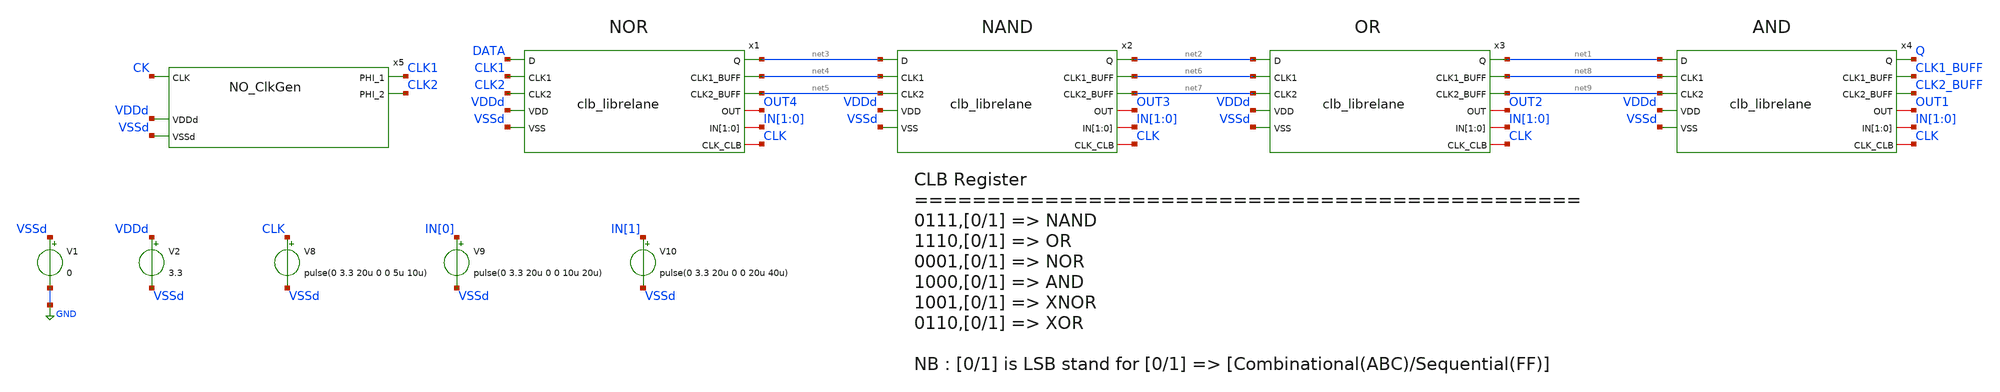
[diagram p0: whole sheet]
** sch_path: designs/libs/tb_fpga/tb_clb/tb_clb.sch
**.subckt tb_clb
V1 VSSd GND 0
V2 VDDd VSSd 3.3
V8 CLK VSSd pulse(0 3.3 20u 0 0 5u 10u)
V9 IN[0] VSSd pulse(0 3.3 20u 0 0 10u 20u)
V10 IN[1] VSSd pulse(0 3.3 20u 0 0 20u 40u)
x5 CLK2 CK CLK1 VDDd VSSd NO_ClkGen
x1 DATA CLK1 CLK2 VDDd VSSd net3 net4 net5 OUT4 IN[1] IN[0] CLK clb_librelane
x2 net3 net4 net5 VDDd VSSd net2 net6 net7 OUT3 IN[1] IN[0] CLK clb_librelane
x3 net2 net6 net7 VDDd VSSd net1 net8 net9 OUT2 IN[1] IN[0] CLK clb_librelane
x4 net1 net8 net9 VDDd VSSd Q CLK1_BUFF CLK2_BUFF OUT1 IN[1] IN[0] CLK clb_librelane
**** begin user architecture code


* clock
abit [ bit_node ]  input_vector
.model input_vector
+ d_source(input_file="/foss/designs/sscs-chipathon2025-LNA/designs/libs/tb_fpga/tb_clb/data.txt")
* data
aclock [ clock_node ] clock_vector
.model clock_vector
+ d_source(input_file="/foss/designs/sscs-chipathon2025-LNA/designs/libs/tb_fpga/tb_clb/data_clk.txt")
* convert digital signals to analog
aconvert [ bit_node clock_node ] [ data ck ] dac_in
.model dac_in dac_bridge (out_low=0V out_high=3.3V t_rise=0.2ns t_fall=0.2ns)

.control
    save all
    TRAN 0.1u 100u
    write tb_clb.raw
.endc



.include /foss/pdks/gf180mcuD/libs.ref/gf180mcu_fd_sc_mcu7t5v0/spice/gf180mcu_fd_sc_mcu7t5v0.spice
.include /foss/pdks/gf180mcuD/libs.ref/gf180mcu_fd_sc_mcu9t5v0/spice/gf180mcu_fd_sc_mcu9t5v0.spice
.include $::180MCU_MODELS/design.ngspice
.lib $::180MCU_MODELS/sm141064.ngspice typical

**** end user architecture code
**.ends

* expanding   symbol:  switch_matrix_gf180mcu_9t5v0/NO_ClkGen/NO_ClkGen.sym # of pins=5
** sym_path: switch_matrix_gf180mcu_9t5v0/NO_ClkGen/NO_ClkGen.sym
** sch_path: switch_matrix_gf180mcu_9t5v0/NO_ClkGen/NO_ClkGen.sch
.subckt NO_ClkGen PHI_2 CLK PHI_1 VDDd VSSd
*.ipin CLK
*.opin PHI_2
*.opin PHI_1
*.iopin VDDd
*.iopin VSSd
x1 OUT_bot_d CLKB VSSd VDDd VSSd VDDd OUT_top gf180mcu_fd_sc_mcu9t5v0__nand2_1
x2 OUT_top_d CLKbuf VSSd VDDd VSSd VDDd OUT_bot gf180mcu_fd_sc_mcu9t5v0__nand2_1
x3 OUT_top VSSd VDDd VSSd VDDd PHI_2 gf180mcu_fd_sc_mcu9t5v0__inv_1
x4 PHI_2 VSSd VDDd VSSd VDDd net5 gf180mcu_fd_sc_mcu9t5v0__inv_1
x5 net3 VSSd VDDd VSSd VDDd net2 gf180mcu_fd_sc_mcu9t5v0__inv_1
x6 OUT_bot VSSd VDDd VSSd VDDd PHI_1 gf180mcu_fd_sc_mcu9t5v0__inv_1
x7 PHI_1 VSSd VDDd VSSd VDDd net6 gf180mcu_fd_sc_mcu9t5v0__inv_1
x8 net4 VSSd VDDd VSSd VDDd net1 gf180mcu_fd_sc_mcu9t5v0__inv_1
x9 CLKB VSSd VDDd VSSd VDDd CLKbuf gf180mcu_fd_sc_mcu9t5v0__inv_1
x10 CLK VSSd VDDd VSSd VDDd CLKB gf180mcu_fd_sc_mcu9t5v0__inv_1
x11 net5 VSSd VDDd VSSd VDDd net3 gf180mcu_fd_sc_mcu9t5v0__inv_1
x12 net6 VSSd VDDd VSSd VDDd net4 gf180mcu_fd_sc_mcu9t5v0__inv_1
x13 net2 VSSd VDDd VSSd VDDd net7 gf180mcu_fd_sc_mcu9t5v0__inv_1
x15 net1 VSSd VDDd VSSd VDDd net8 gf180mcu_fd_sc_mcu9t5v0__inv_1
x17 net7 VSSd VDDd VSSd VDDd net9 gf180mcu_fd_sc_mcu9t5v0__inv_1
x18 net8 VSSd VDDd VSSd VDDd net12 gf180mcu_fd_sc_mcu9t5v0__inv_1
x14 net9 VSSd VDDd VSSd VDDd net10 gf180mcu_fd_sc_mcu9t5v0__inv_1
x16 net12 VSSd VDDd VSSd VDDd net11 gf180mcu_fd_sc_mcu9t5v0__inv_1
x19 net10 VSSd VDDd VSSd VDDd OUT_top_d gf180mcu_fd_sc_mcu9t5v0__inv_1
x20 net11 VSSd VDDd VSSd VDDd OUT_bot_d gf180mcu_fd_sc_mcu9t5v0__inv_1
* noconn VDDd
* noconn VSSd
.ends


* expanding   symbol:  core_fpga/clb_2bit/clb_librelane.sym # of pins=11
** sym_path: designs/libs/core_fpga/clb_2bit/clb_librelane.sym
.include /foss/designs/sscs-chipathon2025-LNA/designs/libs/core_fpga/clb_2bit/clb_librelane.spice
.GLOBAL GND
.end
